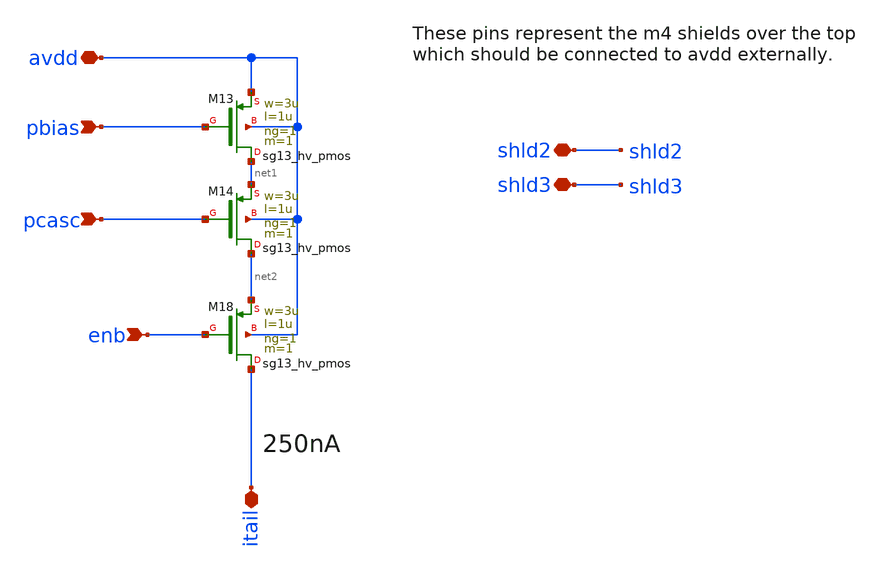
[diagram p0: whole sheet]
** sch_path: xschem/bias_pstack.sch
**.subckt bias_pstack avdd itail enb pcasc pbias shld2 shld3
*.iopin avdd
*.iopin itail
*.ipin enb
*.ipin pcasc
*.ipin pbias
*.iopin shld2
*.iopin shld3
XM13 net1 pbias avdd avdd sg13_hv_pmos w=3u l=1u ng=1 m=1 mm_ok=1
XM18 itail enb net2 avdd sg13_hv_pmos w=3u l=1u ng=1 m=1 mm_ok=1
XM14 net2 pcasc net1 avdd sg13_hv_pmos w=3u l=1u ng=1 m=1 mm_ok=1
**.ends
.end
